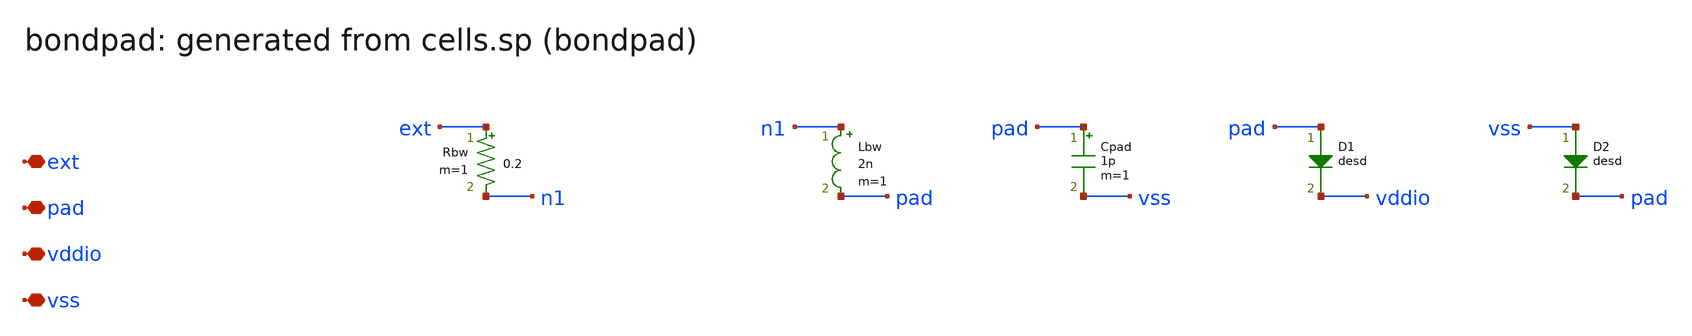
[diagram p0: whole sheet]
** sch_path: sram/xschem/bondpad.sch
**.subckt bondpad ext pad vddio vss
*.iopin ext
*.iopin pad
*.iopin vddio
*.iopin vss
Rbw ext n1 0.2 m=1
Lbw n1 pad 2n m=1
Cpad pad vss 1p m=1
D1 pad vddio desd area=1
D2 vss pad desd area=1
**** begin user architecture code

.model desd D(is=1e-14 cjo=0.2p rs=2)

**** end user architecture code
**.ends
.end
